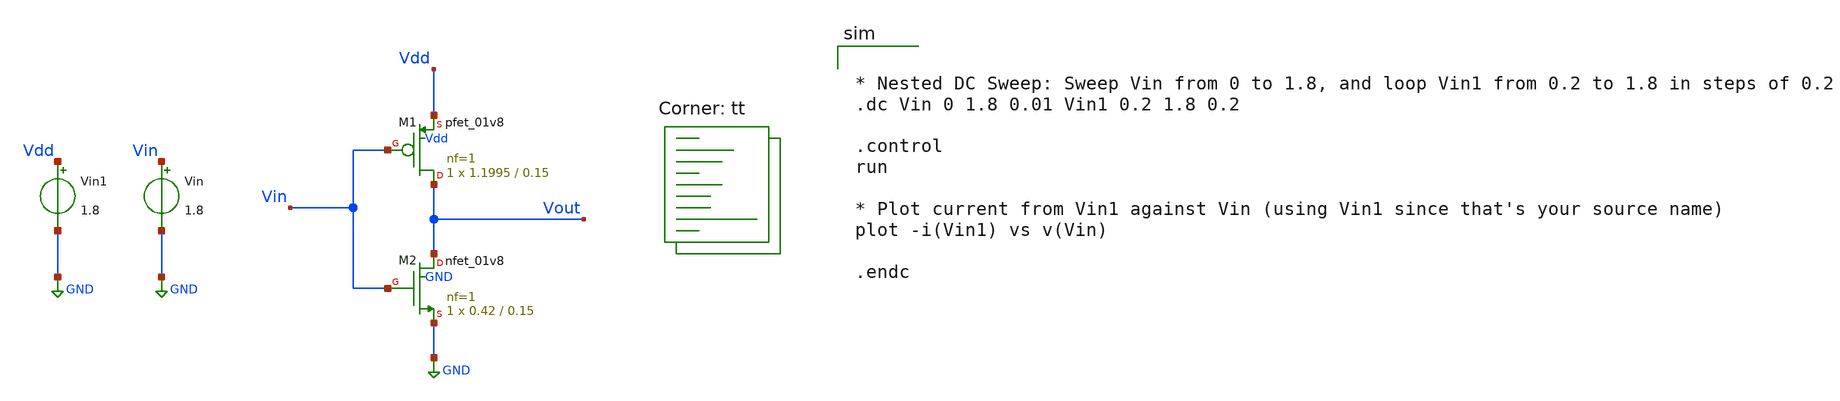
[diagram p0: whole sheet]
** sch_path: assignments/assignment2/assing1c.sch
**.subckt assing1c
Vin Vin GND 1.8
XM1 Vout Vin Vdd Vdd sky130_fd_pr__pfet_01v8 L=0.15 W=1.1995 nf=1 ad='int((nf+1)/2) * W/nf * 0.29' as='int((nf+2)/2) * W/nf * 0.29'
+ pd='2*int((nf+1)/2) * (W/nf + 0.29)' ps='2*int((nf+2)/2) * (W/nf + 0.29)' nrd='0.29 / W' nrs='0.29 / W'
+ sa=0 sb=0 sd=0 mult=1 m=1
XM2 Vout Vin GND GND sky130_fd_pr__nfet_01v8 L=0.15 W=0.42 nf=1 ad='int((nf+1)/2) * W/nf * 0.29' as='int((nf+2)/2) * W/nf * 0.29'
+ pd='2*int((nf+1)/2) * (W/nf + 0.29)' ps='2*int((nf+2)/2) * (W/nf + 0.29)' nrd='0.29 / W' nrs='0.29 / W'
+ sa=0 sb=0 sd=0 mult=1 m=1
Vin1 Vdd GND 1.8
**** begin user architecture code


* Nested DC Sweep: Sweep Vin from 0 to 1.8, and loop Vin1 from 0.2 to 1.8 in steps of 0.2
.dc Vin 0 1.8 0.01 Vin1 0.2 1.8 0.2

.control
run

* Plot current from Vin1 against Vin (using Vin1 since that's your source name)
plot -i(Vin1) vs v(Vin)

.endc


.lib $::SKYWATER_MODELS/sky130.lib.spice tt
**** end user architecture code
**.ends
.GLOBAL GND
.end
